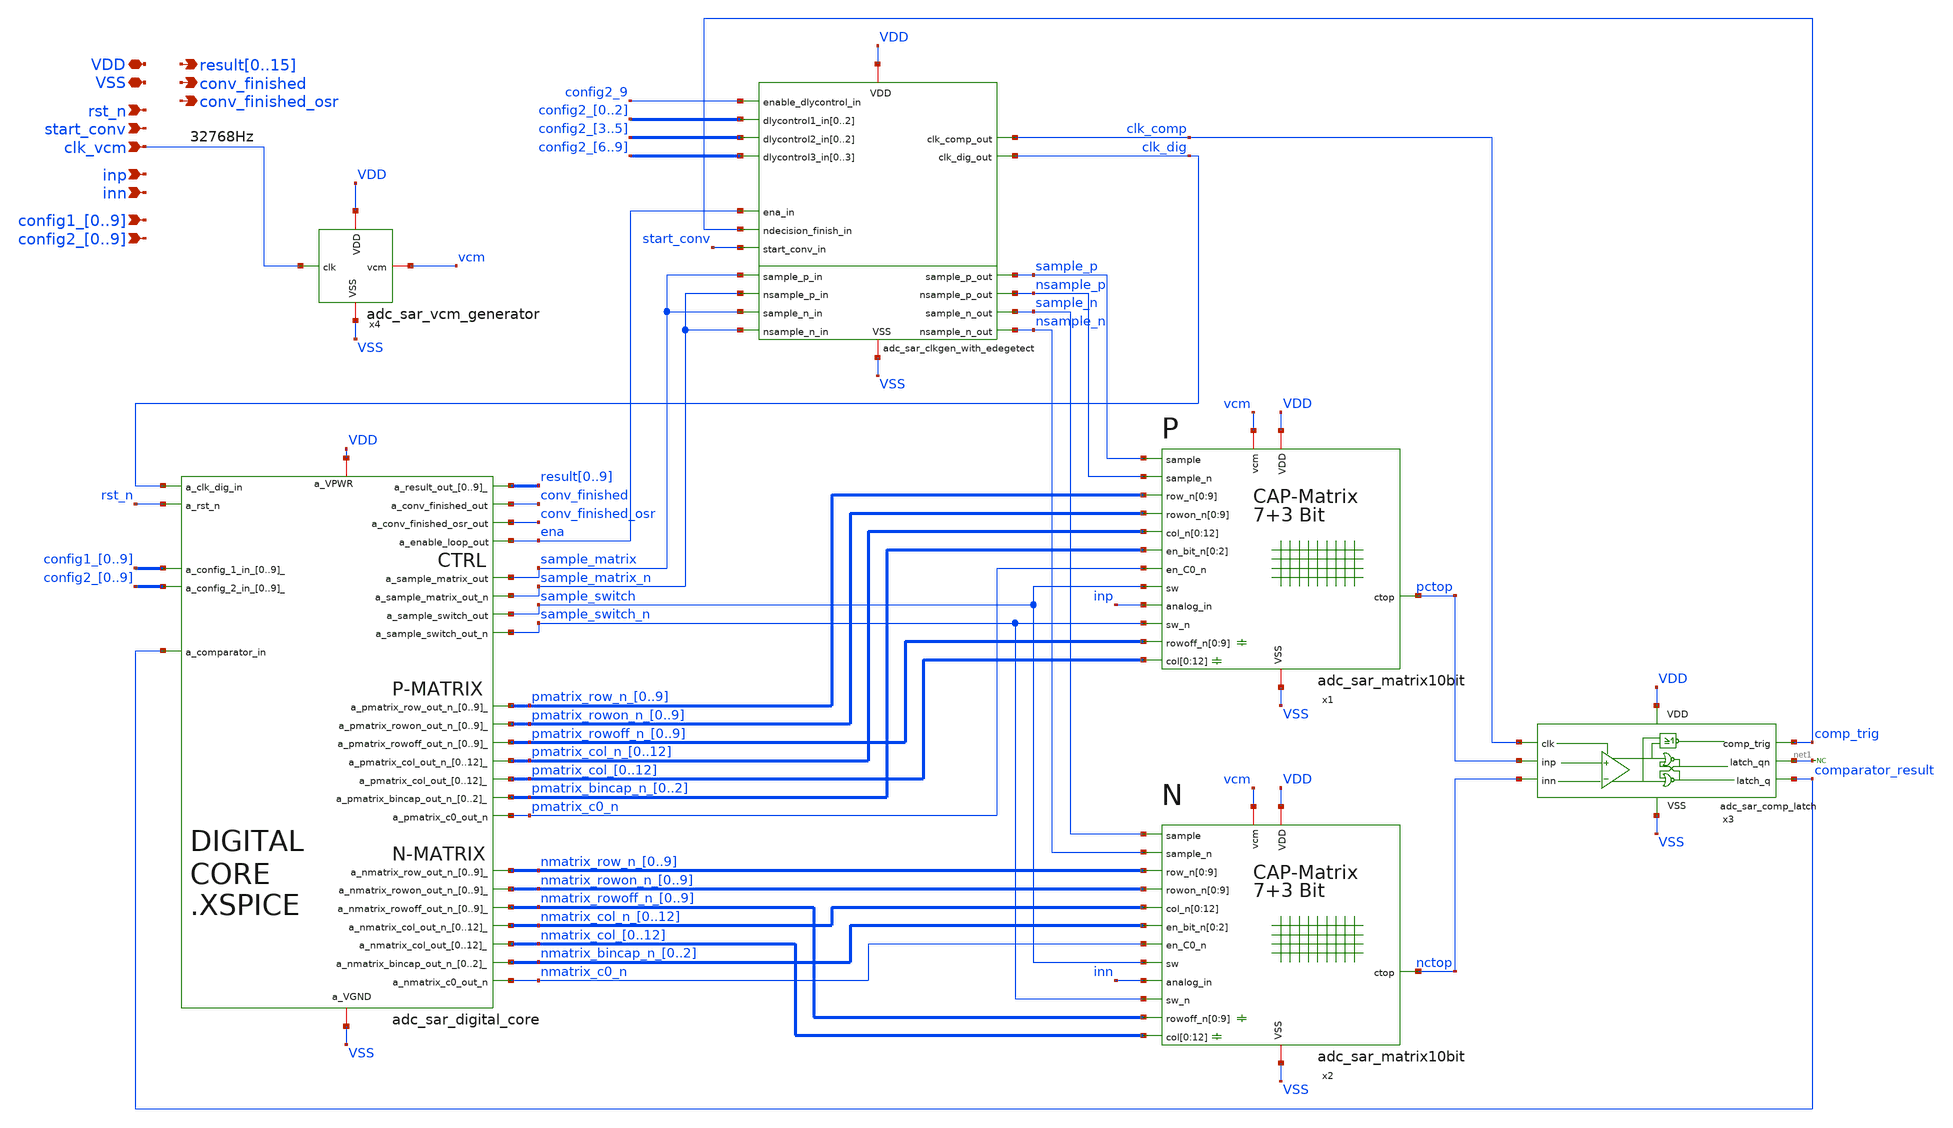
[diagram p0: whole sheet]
** sch_path: adc_sar_top.sch
**.subckt adc_sar_top VDD VSS rst_n start_conv clk_vcm inp inn
*+ config1_0,config1_1,config1_2,config1_3,config1_4,config1_5,config1_6,config1_7,config1_8,config1_9 config2_0,config2_1,config2_2,config2_3,config2_4,config2_5,config2_6,config2_7,config2_8,config2_9
*+ result0,result1,result2,result3,result4,result5,result6,result7,result8,result9,result10,result11,result12,result13,result14,result15 conv_finished conv_finished_osr
*.iopin VDD
*.iopin VSS
*.ipin rst_n
*.ipin start_conv
*.ipin clk_vcm
*.ipin inp
*.ipin inn
*.ipin
*+ config1_0,config1_1,config1_2,config1_3,config1_4,config1_5,config1_6,config1_7,config1_8,config1_9
*.ipin
*+ config2_0,config2_1,config2_2,config2_3,config2_4,config2_5,config2_6,config2_7,config2_8,config2_9
*.opin
*+ result0,result1,result2,result3,result4,result5,result6,result7,result8,result9,result10,result11,result12,result13,result14,result15
*.opin conv_finished
*.opin conv_finished_osr
* noconn #net1
x1 pmatrix_row_n_0 pmatrix_row_n_1 pmatrix_row_n_2 pmatrix_row_n_3 pmatrix_row_n_4 pmatrix_row_n_5
+ pmatrix_row_n_6 pmatrix_row_n_7 pmatrix_row_n_8 pmatrix_row_n_9 pmatrix_rowon_n_0 pmatrix_rowon_n_1
+ pmatrix_rowon_n_2 pmatrix_rowon_n_3 pmatrix_rowon_n_4 pmatrix_rowon_n_5 pmatrix_rowon_n_6 pmatrix_rowon_n_7
+ pmatrix_rowon_n_8 pmatrix_rowon_n_9 pmatrix_rowoff_n_0 pmatrix_rowoff_n_1 pmatrix_rowoff_n_2 pmatrix_rowoff_n_3
+ pmatrix_rowoff_n_4 pmatrix_rowoff_n_5 pmatrix_rowoff_n_6 pmatrix_rowoff_n_7 pmatrix_rowoff_n_8 pmatrix_rowoff_n_9
+ pmatrix_col_n_0 pmatrix_col_n_1 pmatrix_col_n_2 pmatrix_col_n_3 pmatrix_col_n_4 pmatrix_col_n_5 pmatrix_col_n_6
+ pmatrix_col_n_7 pmatrix_col_n_8 pmatrix_col_n_9 pmatrix_col_n_10 pmatrix_col_n_11 pmatrix_col_n_12 pmatrix_col_0
+ pmatrix_col_1 pmatrix_col_2 pmatrix_col_3 pmatrix_col_4 pmatrix_col_5 pmatrix_col_6 pmatrix_col_7 pmatrix_col_8
+ pmatrix_col_9 pmatrix_col_10 pmatrix_col_11 pmatrix_col_12 VDD VSS vcm sample_p nsample_p pmatrix_bincap_n_0
+ pmatrix_bincap_n_1 pmatrix_bincap_n_2 pmatrix_c0_n sample_switch sample_switch_n inp pctop adc_sar_matrix10bit
x2 nmatrix_row_n_0 nmatrix_row_n_1 nmatrix_row_n_2 nmatrix_row_n_3 nmatrix_row_n_4 nmatrix_row_n_5
+ nmatrix_row_n_6 nmatrix_row_n_7 nmatrix_row_n_8 nmatrix_row_n_9 nmatrix_rowon_n_0 nmatrix_rowon_n_1
+ nmatrix_rowon_n_2 nmatrix_rowon_n_3 nmatrix_rowon_n_4 nmatrix_rowon_n_5 nmatrix_rowon_n_6 nmatrix_rowon_n_7
+ nmatrix_rowon_n_8 nmatrix_rowon_n_9 nmatrix_rowoff_n_0 nmatrix_rowoff_n_1 nmatrix_rowoff_n_2 nmatrix_rowoff_n_3
+ nmatrix_rowoff_n_4 nmatrix_rowoff_n_5 nmatrix_rowoff_n_6 nmatrix_rowoff_n_7 nmatrix_rowoff_n_8 nmatrix_rowoff_n_9
+ nmatrix_col_n_0 nmatrix_col_n_1 nmatrix_col_n_2 nmatrix_col_n_3 nmatrix_col_n_4 nmatrix_col_n_5 nmatrix_col_n_6
+ nmatrix_col_n_7 nmatrix_col_n_8 nmatrix_col_n_9 nmatrix_col_n_10 nmatrix_col_n_11 nmatrix_col_n_12 nmatrix_col_0
+ nmatrix_col_1 nmatrix_col_2 nmatrix_col_3 nmatrix_col_4 nmatrix_col_5 nmatrix_col_6 nmatrix_col_7 nmatrix_col_8
+ nmatrix_col_9 nmatrix_col_10 nmatrix_col_11 nmatrix_col_12 VDD VSS vcm sample_n nsample_n nmatrix_bincap_n_0
+ nmatrix_bincap_n_1 nmatrix_bincap_n_2 nmatrix_c0_n sample_switch sample_switch_n inn nctop adc_sar_matrix10bit
x3 VDD VSS clk_comp pctop nctop comp_trig net1 comparator_result adc_sar_comp_latch
x4 VDD vcm clk_vcm VSS adc_sar_vcm_generator
**.ends
.end
